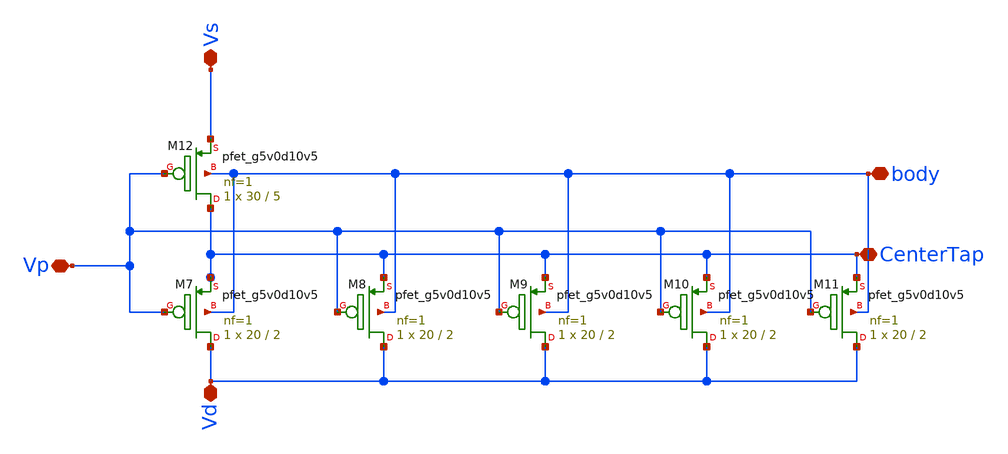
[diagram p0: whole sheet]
** sch_path: xschem/PrimalStructures/PMOSPair.sch
**.subckt PMOSPair Vp Vs body Vd CenterTap
*.iopin Vp
*.iopin Vs
*.iopin body
*.iopin Vd
*.iopin CenterTap
XM7 Vd Vp CenterTap body sky130_fd_pr__pfet_g5v0d10v5 L=2 W=20 nf=1 ad='int((nf+1)/2) * W/nf * 0.29'
+ as='int((nf+2)/2) * W/nf * 0.29' pd='2*int((nf+1)/2) * (W/nf + 0.29)' ps='2*int((nf+2)/2) * (W/nf + 0.29)'
+ nrd='0.29 / W' nrs='0.29 / W' sa=0 sb=0 sd=0 mult=1 m=1
XM8 Vd Vp CenterTap body sky130_fd_pr__pfet_g5v0d10v5 L=2 W=20 nf=1 ad='int((nf+1)/2) * W/nf * 0.29'
+ as='int((nf+2)/2) * W/nf * 0.29' pd='2*int((nf+1)/2) * (W/nf + 0.29)' ps='2*int((nf+2)/2) * (W/nf + 0.29)'
+ nrd='0.29 / W' nrs='0.29 / W' sa=0 sb=0 sd=0 mult=1 m=1
XM9 Vd Vp CenterTap body sky130_fd_pr__pfet_g5v0d10v5 L=2 W=20 nf=1 ad='int((nf+1)/2) * W/nf * 0.29'
+ as='int((nf+2)/2) * W/nf * 0.29' pd='2*int((nf+1)/2) * (W/nf + 0.29)' ps='2*int((nf+2)/2) * (W/nf + 0.29)'
+ nrd='0.29 / W' nrs='0.29 / W' sa=0 sb=0 sd=0 mult=1 m=1
XM10 Vd Vp CenterTap body sky130_fd_pr__pfet_g5v0d10v5 L=2 W=20 nf=1 ad='int((nf+1)/2) * W/nf * 0.29'
+ as='int((nf+2)/2) * W/nf * 0.29' pd='2*int((nf+1)/2) * (W/nf + 0.29)' ps='2*int((nf+2)/2) * (W/nf + 0.29)'
+ nrd='0.29 / W' nrs='0.29 / W' sa=0 sb=0 sd=0 mult=1 m=1
XM11 Vd Vp CenterTap body sky130_fd_pr__pfet_g5v0d10v5 L=2 W=20 nf=1 ad='int((nf+1)/2) * W/nf * 0.29'
+ as='int((nf+2)/2) * W/nf * 0.29' pd='2*int((nf+1)/2) * (W/nf + 0.29)' ps='2*int((nf+2)/2) * (W/nf + 0.29)'
+ nrd='0.29 / W' nrs='0.29 / W' sa=0 sb=0 sd=0 mult=1 m=1
XM12 CenterTap Vp Vs body sky130_fd_pr__pfet_g5v0d10v5 L=5 W=30 nf=1 ad='int((nf+1)/2) * W/nf * 0.29'
+ as='int((nf+2)/2) * W/nf * 0.29' pd='2*int((nf+1)/2) * (W/nf + 0.29)' ps='2*int((nf+2)/2) * (W/nf + 0.29)'
+ nrd='0.29 / W' nrs='0.29 / W' sa=0 sb=0 sd=0 mult=1 m=1
**** begin user architecture code

** opencircuitdesign pdks install
.lib $::SKYWATER_MODELS/sky130.lib.spice tt


**** end user architecture code
**.ends
.end
